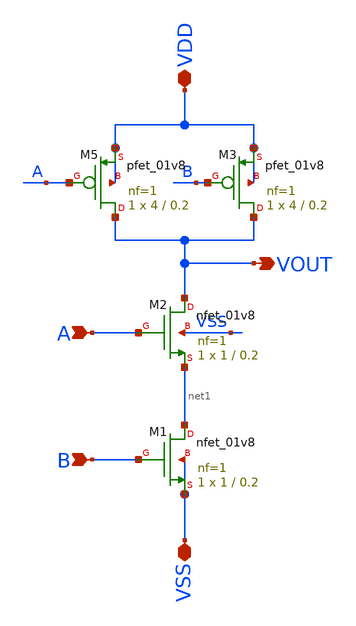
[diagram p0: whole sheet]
** sch_path: Xschem/PLL_TOP_Schematics/NAND.sch
* Copyright 2022 GlobalFoundries PDK Authors
* Licensed under the Apache License, Version 2.0 (the "License");
* you may not use this file except in compliance with the License.
* You may obtain a copy of the License at
* https://www.apache.org/licenses/LICENSE-2.0
* Unless required by applicable law or agreed to in writing, software
* distributed under the License is distributed on an "AS IS" BASIS,
* WITHOUT WARRANTIES OR CONDITIONS OF ANY KIND, either express or implied.
* See the License for the specific language governing permissions and
* limitations under the License.
**.subckt NAND VDD VSS A B VOUT
*.iopin VDD
*.iopin VSS
*.ipin A
*.ipin B
*.opin VOUT
XM5 VOUT A VDD VDD sky130_fd_pr__pfet_01v8 L=0.2 W=4 nf=1 ad='int((nf+1)/2) * W/nf * 0.29' as='int((nf+2)/2) * W/nf * 0.29'
+ pd='2*int((nf+1)/2) * (W/nf + 0.29)' ps='2*int((nf+2)/2) * (W/nf + 0.29)' nrd='0.29 / W' nrs='0.29 / W'
+ sa=0 sb=0 sd=0 mult=1 m=1
XM1 net1 B VSS VSS sky130_fd_pr__nfet_01v8 L=0.2 W=1 nf=1 ad='int((nf+1)/2) * W/nf * 0.29' as='int((nf+2)/2) * W/nf * 0.29'
+ pd='2*int((nf+1)/2) * (W/nf + 0.29)' ps='2*int((nf+2)/2) * (W/nf + 0.29)' nrd='0.29 / W' nrs='0.29 / W'
+ sa=0 sb=0 sd=0 mult=1 m=1
XM2 VOUT A net1 VSS sky130_fd_pr__nfet_01v8 L=0.2 W=1 nf=1 ad='int((nf+1)/2) * W/nf * 0.29' as='int((nf+2)/2) * W/nf * 0.29'
+ pd='2*int((nf+1)/2) * (W/nf + 0.29)' ps='2*int((nf+2)/2) * (W/nf + 0.29)' nrd='0.29 / W' nrs='0.29 / W'
+ sa=0 sb=0 sd=0 mult=1 m=1
XM3 VOUT B VDD VDD sky130_fd_pr__pfet_01v8 L=0.2 W=4 nf=1 ad='int((nf+1)/2) * W/nf * 0.29' as='int((nf+2)/2) * W/nf * 0.29'
+ pd='2*int((nf+1)/2) * (W/nf + 0.29)' ps='2*int((nf+2)/2) * (W/nf + 0.29)' nrd='0.29 / W' nrs='0.29 / W'
+ sa=0 sb=0 sd=0 mult=1 m=1
**.ends
.end
